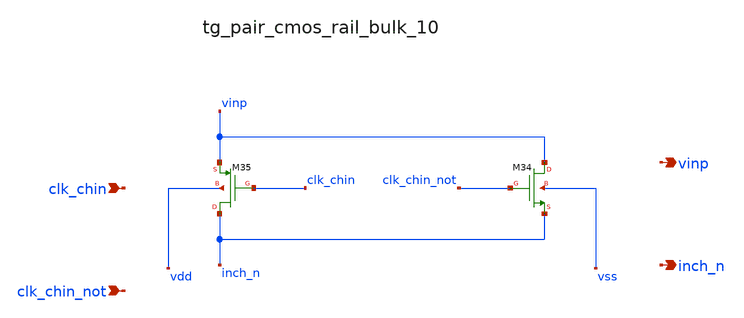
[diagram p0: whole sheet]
** sch_path: analog-db/raw/ia_002_fan_chopper_simple/hier/blocks/tg_pair_cmos_rail_bulk_10.sch
**.subckt tg_pair_cmos_rail_bulk_10 clk_chin clk_chin_not vinp inch_n
*.ipin clk_chin
*.ipin clk_chin_not
*.opin vinp
*.opin inch_n
XM34 vinp clk_chin_not inch_n vss sg13_lv_nmos w=x_dut_xm34_w l=x_dut_xm34_l ng=1 m=x_dut_xm34_m
XM35 inch_n clk_chin vinp vdd sg13_lv_pmos w=x_dut_xm35_w l=x_dut_xm35_l ng=1 m=x_dut_xm35_m
**.ends
.end
